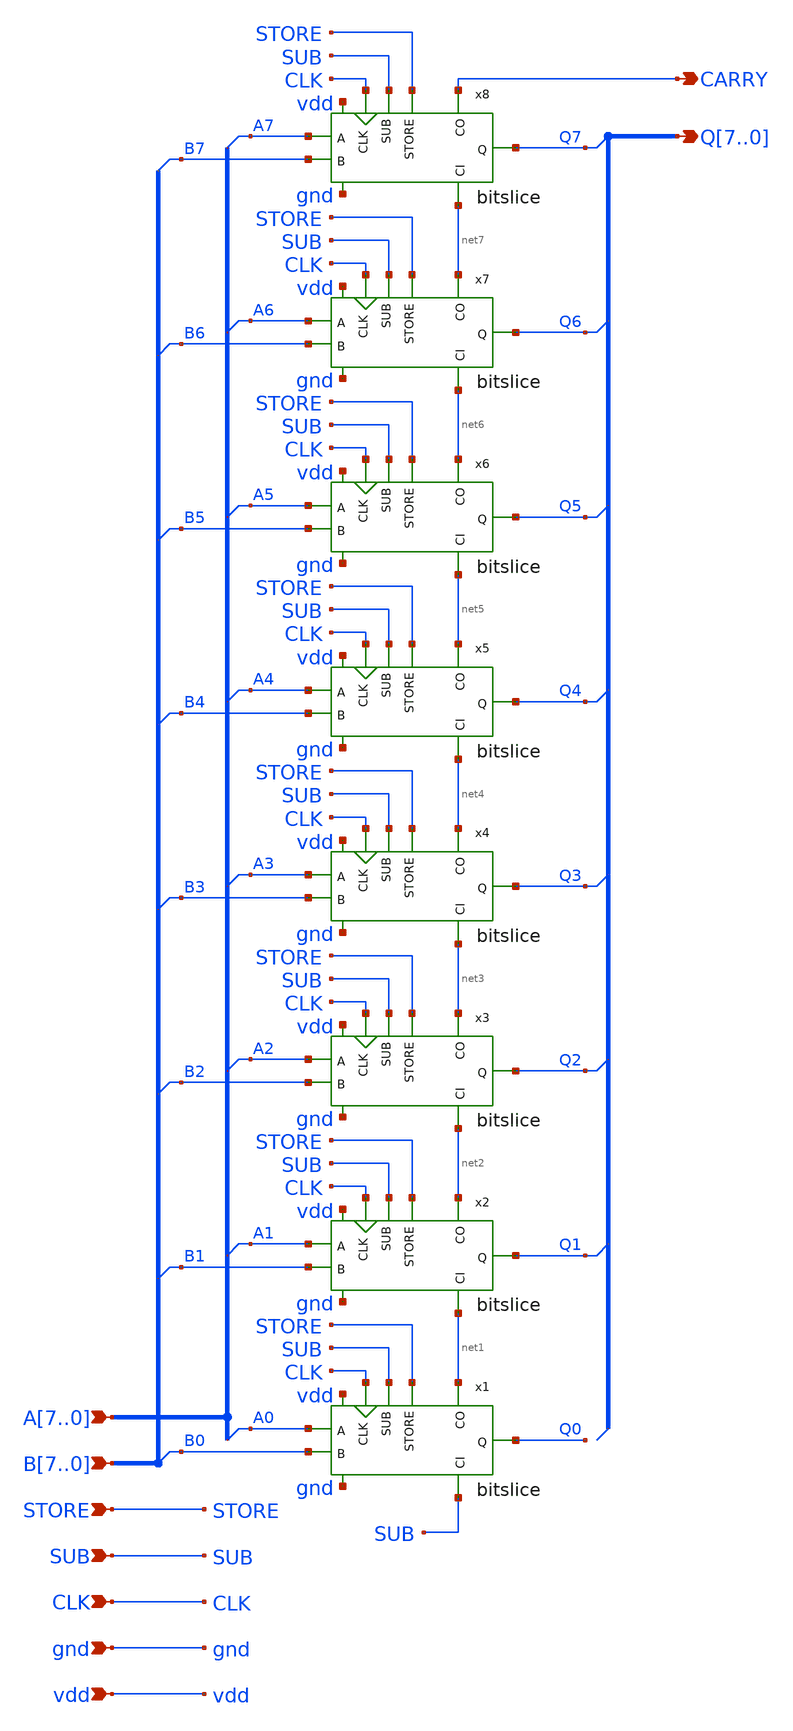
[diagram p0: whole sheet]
** sch_path: xschem/datapath.sch
**.subckt datapath A7,A6,A5,A4,A3,A2,A1,A0 B7,B6,B5,B4,B3,B2,B1,B0 Q7,Q6,Q5,Q4,Q3,Q2,Q1,Q0 STORE SUB
*+ CLK CARRY vdd gnd
*.ipin A7,A6,A5,A4,A3,A2,A1,A0
*.ipin B7,B6,B5,B4,B3,B2,B1,B0
*.opin Q7,Q6,Q5,Q4,Q3,Q2,Q1,Q0
*.ipin STORE
*.ipin SUB
*.ipin CLK
*.opin CARRY
*.ipin vdd
*.ipin gnd
x1 net1 SUB CLK STORE A0 Q0 B0 SUB vdd gnd bitslice
x2 net2 SUB CLK STORE A1 Q1 B1 net1 vdd gnd bitslice
x3 net3 SUB CLK STORE A2 Q2 B2 net2 vdd gnd bitslice
x4 net4 SUB CLK STORE A3 Q3 B3 net3 vdd gnd bitslice
x5 net5 SUB CLK STORE A4 Q4 B4 net4 vdd gnd bitslice
x6 net6 SUB CLK STORE A5 Q5 B5 net5 vdd gnd bitslice
x7 net7 SUB CLK STORE A6 Q6 B6 net6 vdd gnd bitslice
x8 CARRY SUB CLK STORE A7 Q7 B7 net7 vdd gnd bitslice
**.ends
.end
